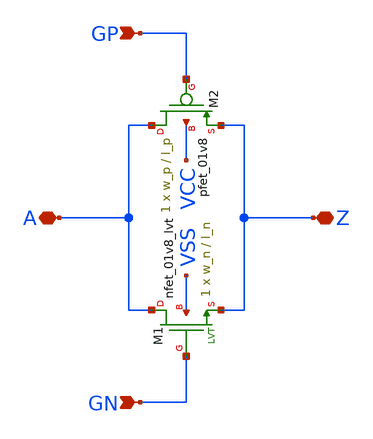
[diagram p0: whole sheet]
** sch_path: sky130_tests_X/passgate_nlvt.sch
* Copyright 2020 Stefan Frederik Schippers
* Licensed under the Apache License, Version 2.0 (the "License");
* you may not use this file except in compliance with the License.
* You may obtain a copy of the License at
* https://www.apache.org/licenses/LICENSE-2.0
* Unless required by applicable law or agreed to in writing, software
* distributed under the License is distributed on an "AS IS" BASIS,
* WITHOUT WARRANTIES OR CONDITIONS OF ANY KIND, either express or implied.
* See the License for the specific language governing permissions and
* limitations under the License.
**.subckt passgate_nlvt A Z GP GN
*.iopin A
*.iopin Z
*.ipin GP
*.ipin GN
XM1 A GN Z VSS sky130_fd_pr__nfet_01v8_lvt w=w_n l=l_n ad=ad pd=pd as=as ps=ps nrd=0 nrs=0 sa=0 sb=0
+ sd=0 nf=1 mult=1 m=1
XM2 A GP Z VCC sky130_fd_pr__pfet_01v8 w=w_p l=l_p ad=ad pd=pd as=as ps=ps nrd=0 nrs=0 sa=0 sb=0
+ sd=0 nf=1 mult=1 m=1
**.ends
.end
